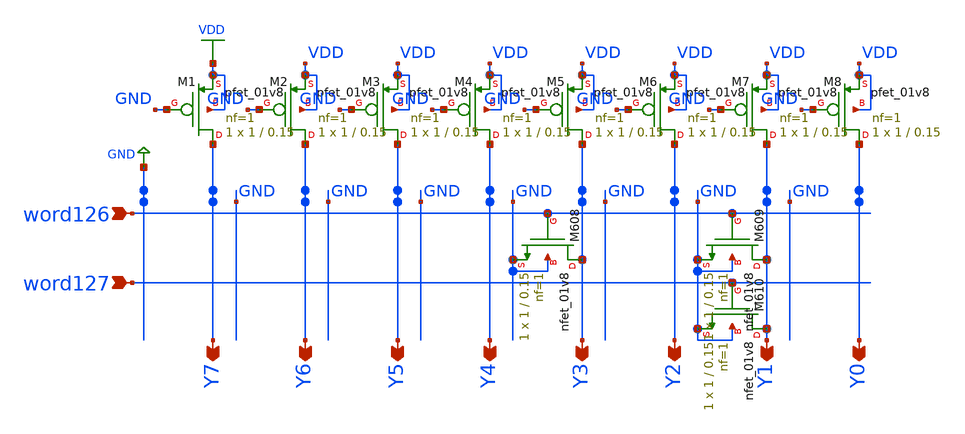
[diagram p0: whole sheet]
** sch_path: circuits/scripts/schematics/memory_last_2.sch
**.subckt memory_last_2 word126 word127 Y7 Y6 Y5 Y4 Y3 Y2 Y1 Y0
*.ipin word126
*.ipin word127
*.opin Y7
*.opin Y6
*.opin Y5
*.opin Y4
*.opin Y3
*.opin Y2
*.opin Y1
*.opin Y0
XM1 Y7 GND VDD VDD sky130_fd_pr__pfet_01v8 L=0.15 W=1 nf=1 ad='int((nf+1)/2) * W/nf * 0.29' as='int((nf+2)/2) * W/nf * 0.29'
+ pd='2*int((nf+1)/2) * (W/nf + 0.29)' ps='2*int((nf+2)/2) * (W/nf + 0.29)' nrd='0.29 / W' nrs='0.29 / W'
+ sa=0 sb=0 sd=0 mult=1 m=1
XM2 Y6 GND VDD VDD sky130_fd_pr__pfet_01v8 L=0.15 W=1 nf=1 ad='int((nf+1)/2) * W/nf * 0.29' as='int((nf+2)/2) * W/nf * 0.29'
+ pd='2*int((nf+1)/2) * (W/nf + 0.29)' ps='2*int((nf+2)/2) * (W/nf + 0.29)' nrd='0.29 / W' nrs='0.29 / W'
+ sa=0 sb=0 sd=0 mult=1 m=1
XM3 Y5 GND VDD VDD sky130_fd_pr__pfet_01v8 L=0.15 W=1 nf=1 ad='int((nf+1)/2) * W/nf * 0.29' as='int((nf+2)/2) * W/nf * 0.29'
+ pd='2*int((nf+1)/2) * (W/nf + 0.29)' ps='2*int((nf+2)/2) * (W/nf + 0.29)' nrd='0.29 / W' nrs='0.29 / W'
+ sa=0 sb=0 sd=0 mult=1 m=1
XM4 Y4 GND VDD VDD sky130_fd_pr__pfet_01v8 L=0.15 W=1 nf=1 ad='int((nf+1)/2) * W/nf * 0.29' as='int((nf+2)/2) * W/nf * 0.29'
+ pd='2*int((nf+1)/2) * (W/nf + 0.29)' ps='2*int((nf+2)/2) * (W/nf + 0.29)' nrd='0.29 / W' nrs='0.29 / W'
+ sa=0 sb=0 sd=0 mult=1 m=1
XM5 Y3 GND VDD VDD sky130_fd_pr__pfet_01v8 L=0.15 W=1 nf=1 ad='int((nf+1)/2) * W/nf * 0.29' as='int((nf+2)/2) * W/nf * 0.29'
+ pd='2*int((nf+1)/2) * (W/nf + 0.29)' ps='2*int((nf+2)/2) * (W/nf + 0.29)' nrd='0.29 / W' nrs='0.29 / W'
+ sa=0 sb=0 sd=0 mult=1 m=1
XM6 Y2 GND VDD VDD sky130_fd_pr__pfet_01v8 L=0.15 W=1 nf=1 ad='int((nf+1)/2) * W/nf * 0.29' as='int((nf+2)/2) * W/nf * 0.29'
+ pd='2*int((nf+1)/2) * (W/nf + 0.29)' ps='2*int((nf+2)/2) * (W/nf + 0.29)' nrd='0.29 / W' nrs='0.29 / W'
+ sa=0 sb=0 sd=0 mult=1 m=1
XM7 Y1 GND VDD VDD sky130_fd_pr__pfet_01v8 L=0.15 W=1 nf=1 ad='int((nf+1)/2) * W/nf * 0.29' as='int((nf+2)/2) * W/nf * 0.29'
+ pd='2*int((nf+1)/2) * (W/nf + 0.29)' ps='2*int((nf+2)/2) * (W/nf + 0.29)' nrd='0.29 / W' nrs='0.29 / W'
+ sa=0 sb=0 sd=0 mult=1 m=1
XM8 Y0 GND VDD VDD sky130_fd_pr__pfet_01v8 L=0.15 W=1 nf=1 ad='int((nf+1)/2) * W/nf * 0.29' as='int((nf+2)/2) * W/nf * 0.29'
+ pd='2*int((nf+1)/2) * (W/nf + 0.29)' ps='2*int((nf+2)/2) * (W/nf + 0.29)' nrd='0.29 / W' nrs='0.29 / W'
+ sa=0 sb=0 sd=0 mult=1 m=1
XM608 Y3 word126 GND GND sky130_fd_pr__nfet_01v8 L=0.15 W=1 nf=1 ad='int((nf+1)/2) * W/nf * 0.29' as='int((nf+2)/2) * W/nf * 0.29'
+ pd='2*int((nf+1)/2) * (W/nf + 0.29)' ps='2*int((nf+2)/2) * (W/nf + 0.29)' nrd='0.29 / W' nrs='0.29 / W'
+ sa=0 sb=0 sd=0 mult=1 m=1
XM609 Y1 word126 GND GND sky130_fd_pr__nfet_01v8 L=0.15 W=1 nf=1 ad='int((nf+1)/2) * W/nf * 0.29' as='int((nf+2)/2) * W/nf * 0.29'
+ pd='2*int((nf+1)/2) * (W/nf + 0.29)' ps='2*int((nf+2)/2) * (W/nf + 0.29)' nrd='0.29 / W' nrs='0.29 / W'
+ sa=0 sb=0 sd=0 mult=1 m=1
XM610 Y1 word127 GND GND sky130_fd_pr__nfet_01v8 L=0.15 W=1 nf=1 ad='int((nf+1)/2) * W/nf * 0.29' as='int((nf+2)/2) * W/nf * 0.29'
+ pd='2*int((nf+1)/2) * (W/nf + 0.29)' ps='2*int((nf+2)/2) * (W/nf + 0.29)' nrd='0.29 / W' nrs='0.29 / W'
+ sa=0 sb=0 sd=0 mult=1 m=1
**.ends
.GLOBAL GND
.GLOBAL VDD
.end
